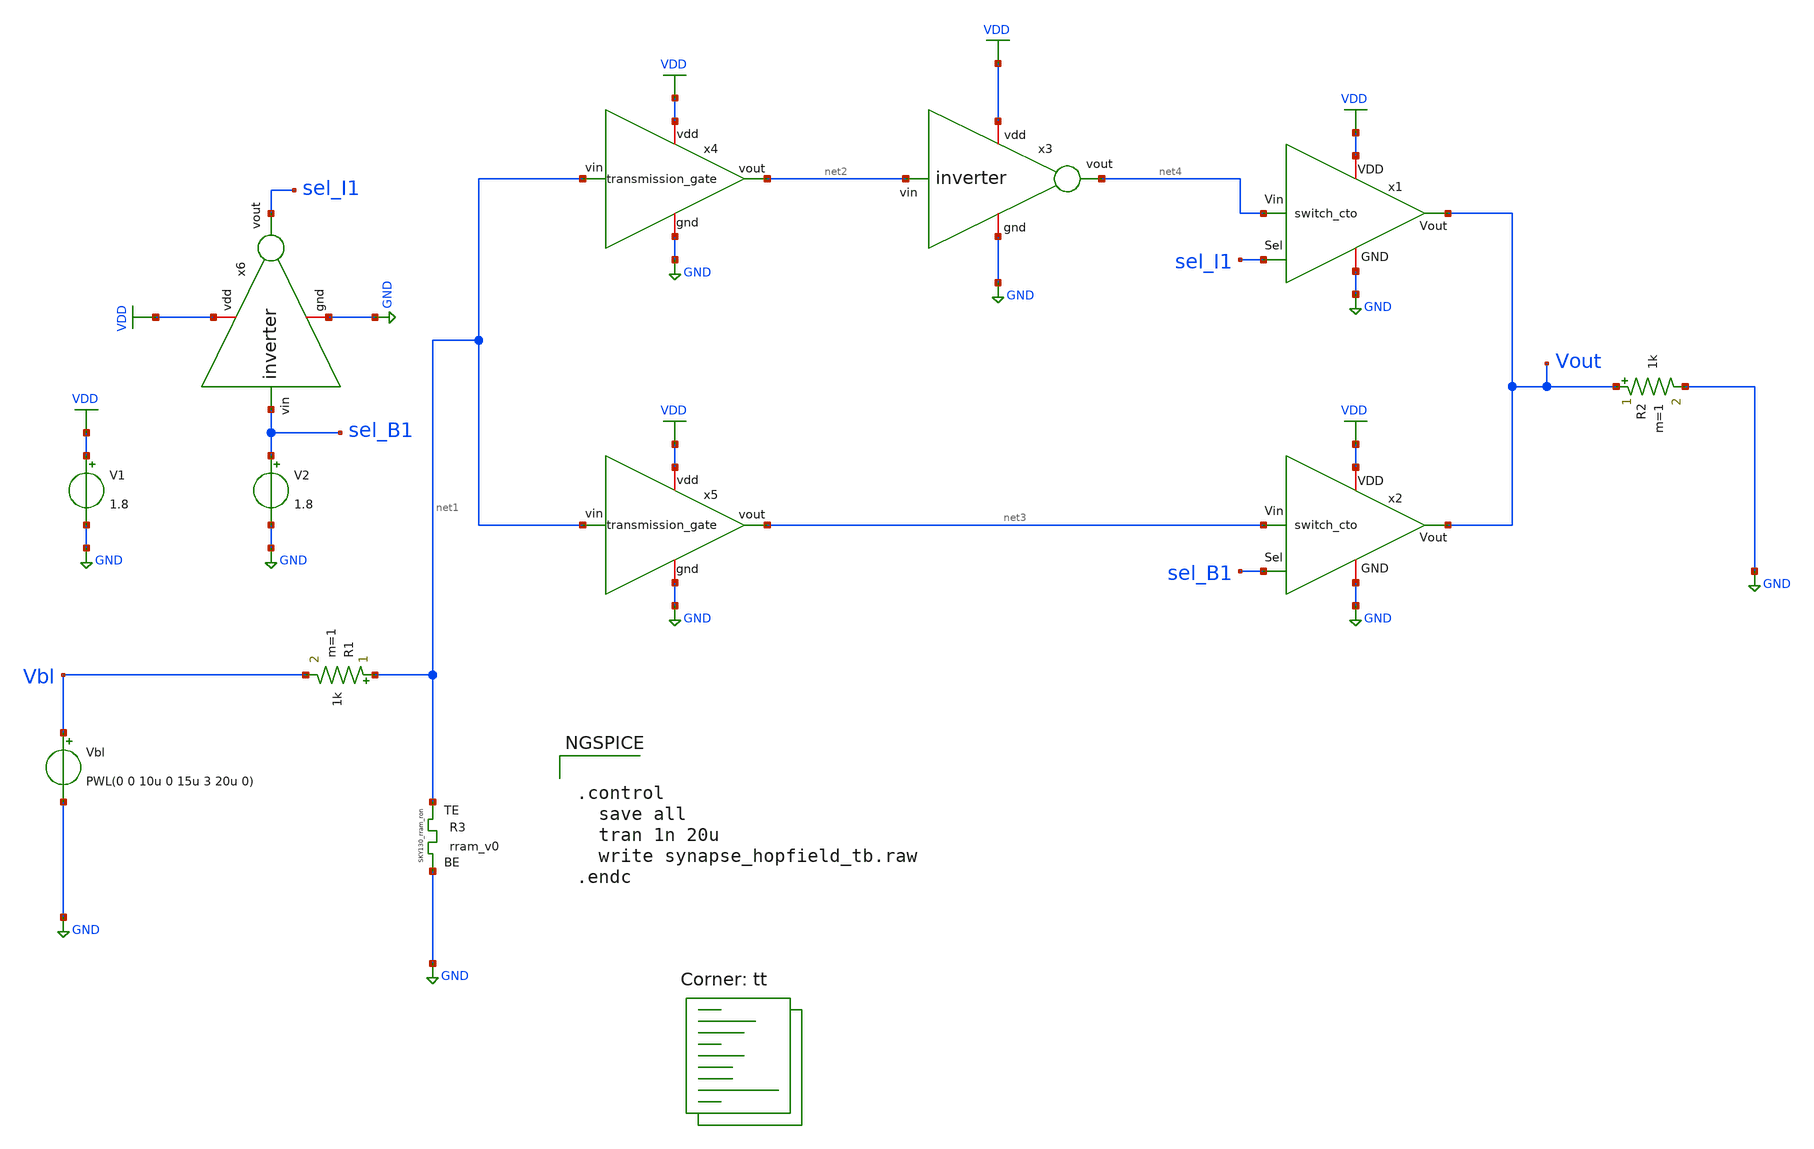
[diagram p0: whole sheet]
** sch_path: hopfield/synapse_hopfield_tb.sch
**.subckt synapse_hopfield_tb
R1 net1 Vbl 1k m=1
R2 Vout GND 1k m=1
x3 VDD net4 net2 GND inverter
XR3 net1 GND rram_v0
V1 VDD GND 1.8
Vbl Vbl GND PWL(0 0 10u 0 15u 3 20u 0)
x4 net1 GND VDD net2 transmission_gate
x5 net1 GND VDD net3 transmission_gate
x1 VDD GND sel_I1 Vout net4 switch_cto
x2 VDD GND sel_B1 Vout net3 switch_cto
V2 sel_B1 GND 1.8
x6 VDD sel_I1 sel_B1 GND inverter
**** begin user architecture code


.control
  save all
  tran 1n 20u
  write synapse_hopfield_tb.raw
.endc



.lib $::SKYWATER_MODELS/sky130.lib.spice tt

** opencircuitdesign pdks install
.inc $::SKYWATER_MODELS/rram_v0.spice

**** end user architecture code
**.ends
.GLOBAL GND
.GLOBAL VDD
.end
